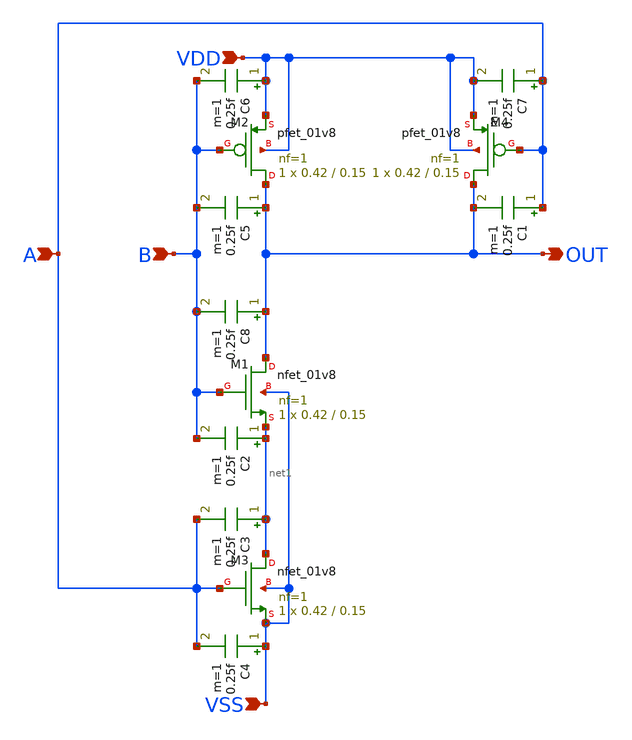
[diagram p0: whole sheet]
** sch_path: mySAR_SKY130/xschem/nand.sch
**.subckt nand B OUT A VDD VSS
*.ipin B
*.opin OUT
*.ipin A
*.ipin VDD
*.ipin VSS
XM2 OUT B VDD VDD sky130_fd_pr__pfet_01v8 L=0.15 W=0.42 nf=1 ad='int((nf+1)/2) * W/nf * 0.29' as='int((nf+2)/2) * W/nf * 0.29'
+ pd='2*int((nf+1)/2) * (W/nf + 0.29)' ps='2*int((nf+2)/2) * (W/nf + 0.29)' nrd='0.29 / W' nrs='0.29 / W'
+ sa=0 sb=0 sd=0 mult=1 m=1
XM1 OUT B net1 VSS sky130_fd_pr__nfet_01v8 L=0.15 W=0.42 nf=1 ad='int((nf+1)/2) * W/nf * 0.29' as='int((nf+2)/2) * W/nf * 0.29'
+ pd='2*int((nf+1)/2) * (W/nf + 0.29)' ps='2*int((nf+2)/2) * (W/nf + 0.29)' nrd='0.29 / W' nrs='0.29 / W'
+ sa=0 sb=0 sd=0 mult=1 m=1
XM3 net1 A VSS VSS sky130_fd_pr__nfet_01v8 L=0.15 W=0.42 nf=1 ad='int((nf+1)/2) * W/nf * 0.29' as='int((nf+2)/2) * W/nf * 0.29'
+ pd='2*int((nf+1)/2) * (W/nf + 0.29)' ps='2*int((nf+2)/2) * (W/nf + 0.29)' nrd='0.29 / W' nrs='0.29 / W'
+ sa=0 sb=0 sd=0 mult=1 m=1
XM4 OUT A VDD VDD sky130_fd_pr__pfet_01v8 L=0.15 W=0.42 nf=1 ad='int((nf+1)/2) * W/nf * 0.29' as='int((nf+2)/2) * W/nf * 0.29'
+ pd='2*int((nf+1)/2) * (W/nf + 0.29)' ps='2*int((nf+2)/2) * (W/nf + 0.29)' nrd='0.29 / W' nrs='0.29 / W'
+ sa=0 sb=0 sd=0 mult=1 m=1
C1 A OUT 0.25f m=1
C2 net1 B 0.25f m=1
C3 net1 A 0.25f m=1
C4 VSS A 0.25f m=1
C5 OUT B 0.25f m=1
C6 VDD B 0.25f m=1
C7 A VDD 0.25f m=1
C8 OUT B 0.25f m=1
**.ends
.end
